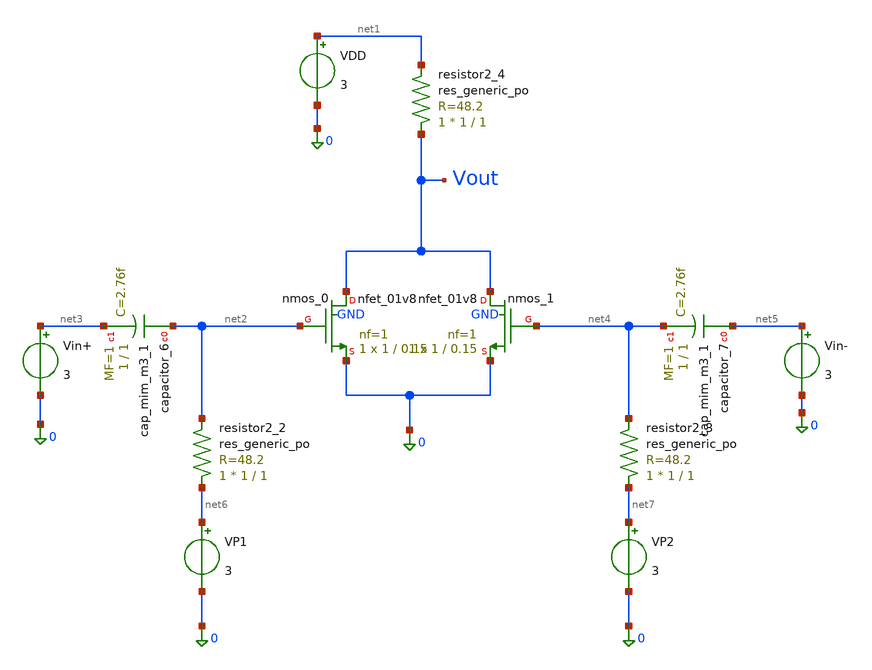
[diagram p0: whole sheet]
** sch_path: golden_netlists/10_1109_ACCESS_2021_3064007_05_003.sch
**.subckt 10_1109_ACCESS_2021_3064007_05_003
Xcapacitor_6 net2 net3 sky130_fd_pr__cap_mim_m3_1 W=1 L=1 MF=1 m=1
Xcapacitor_7 net5 net4 sky130_fd_pr__cap_mim_m3_1 W=1 L=1 MF=1 m=1
Xnmos_0 Vout net2 0 GND sky130_fd_pr__nfet_01v8 L=0.15 W=1 nf=1 ad='int((nf+1)/2) * W/nf * 0.29' as='int((nf+2)/2) * W/nf * 0.29'
+ pd='2*int((nf+1)/2) * (W/nf + 0.29)' ps='2*int((nf+2)/2) * (W/nf + 0.29)' nrd='0.29 / W' nrs='0.29 / W'
+ sa=0 sb=0 sd=0 mult=1 m=1
Xnmos_1 Vout net4 0 GND sky130_fd_pr__nfet_01v8 L=0.15 W=1 nf=1 ad='int((nf+1)/2) * W/nf * 0.29' as='int((nf+2)/2) * W/nf * 0.29'
+ pd='2*int((nf+1)/2) * (W/nf + 0.29)' ps='2*int((nf+2)/2) * (W/nf + 0.29)' nrd='0.29 / W' nrs='0.29 / W'
+ sa=0 sb=0 sd=0 mult=1 m=1
Xresistor2_2 net6 net2 sky130_fd_pr__res_generic_po W=1 L=1 m=1
Xresistor2_3 net7 net4 sky130_fd_pr__res_generic_po W=1 L=1 m=1
Xresistor2_4 Vout net1 sky130_fd_pr__res_generic_po W=1 L=1 m=1
VDD net1 0 3
Vin+ net3 0 3
Vin- net5 0 3
VP1 net6 0 3
VP2 net7 0 3
**.ends
.end
